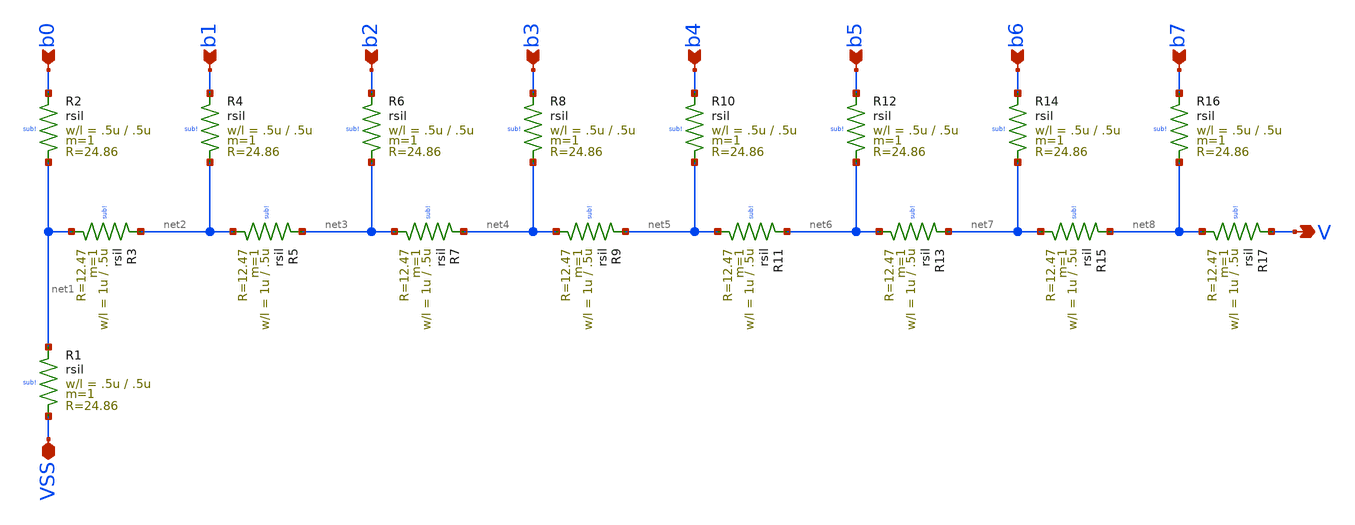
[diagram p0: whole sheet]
** sch_path: xschem/r2r.sch
**.subckt r2r VSS b0 b1 b2 b3 b4 b5 b6 b7 V
*.iopin VSS
*.ipin b0
*.ipin b1
*.ipin b2
*.ipin b3
*.ipin b4
*.ipin b5
*.ipin b6
*.ipin b7
*.opin V
XR1 net1 VSS sub! rsil w=.5u l=.5u m=1 mm_ok=1
XR2 b0 net1 sub! rsil w=.5u l=.5u m=1 mm_ok=1
XR3 net2 net1 sub! rsil w=1u l=.5u m=1 mm_ok=1
XR4 b1 net2 sub! rsil w=.5u l=.5u m=1 mm_ok=1
XR5 net3 net2 sub! rsil w=1u l=.5u m=1 mm_ok=1
XR6 b2 net3 sub! rsil w=.5u l=.5u m=1 mm_ok=1
XR7 net4 net3 sub! rsil w=1u l=.5u m=1 mm_ok=1
XR8 b3 net4 sub! rsil w=.5u l=.5u m=1 mm_ok=1
XR9 net5 net4 sub! rsil w=1u l=.5u m=1 mm_ok=1
XR10 b4 net5 sub! rsil w=.5u l=.5u m=1 mm_ok=1
XR11 net6 net5 sub! rsil w=1u l=.5u m=1 mm_ok=1
XR12 b5 net6 sub! rsil w=.5u l=.5u m=1 mm_ok=1
XR13 net7 net6 sub! rsil w=1u l=.5u m=1 mm_ok=1
XR14 b6 net7 sub! rsil w=.5u l=.5u m=1 mm_ok=1
XR15 net8 net7 sub! rsil w=1u l=.5u m=1 mm_ok=1
XR16 b7 net8 sub! rsil w=.5u l=.5u m=1 mm_ok=1
XR17 V net8 sub! rsil w=1u l=.5u m=1 mm_ok=1
**.ends
.end
